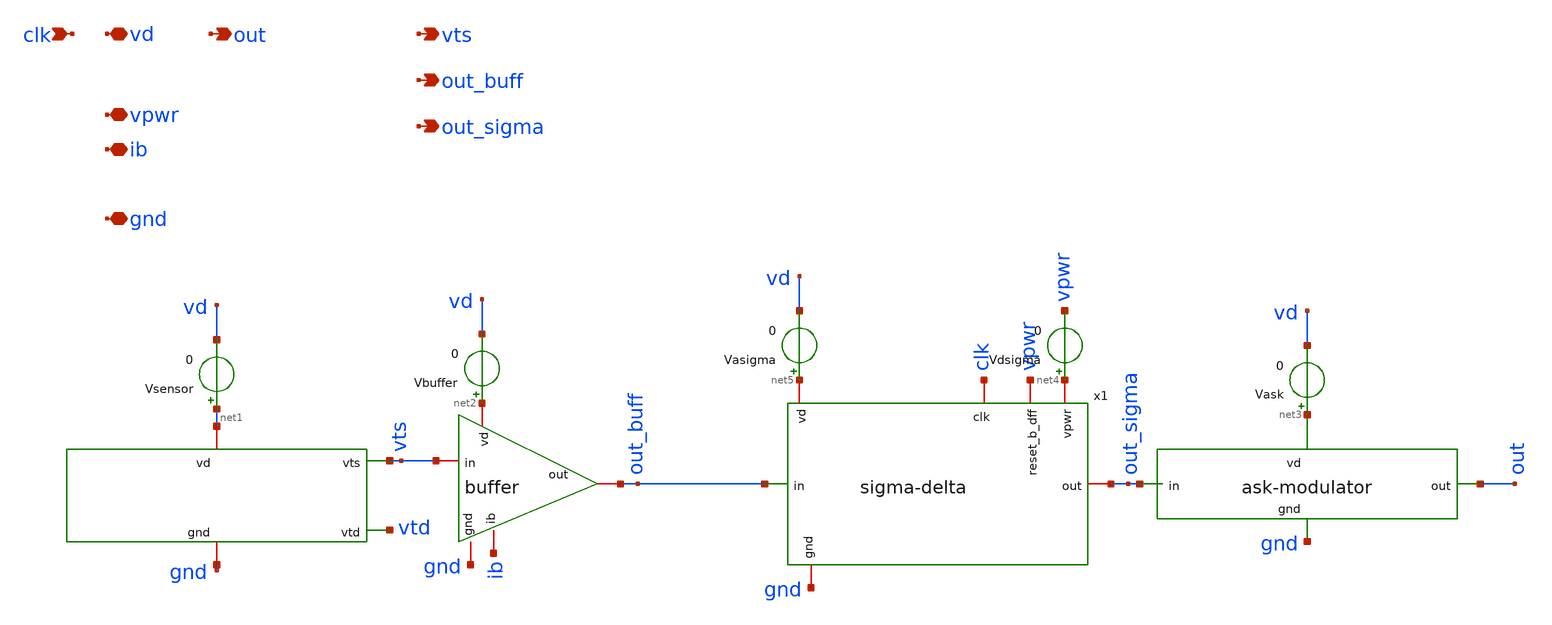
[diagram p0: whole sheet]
** sch_path: device-complete/xschem/device-complete.sch
**.subckt device-complete vd clk out vpwr ib gnd vts out_buff out_sigma
*.iopin vd
*.ipin clk
*.opin out
*.iopin vpwr
*.iopin ib
*.iopin gnd
*.opin vts
*.opin out_buff
*.opin out_sigma
x3 net1 vts vtd gnd sensor
X2 net2 vts out_buff ib gnd buffer
x4 net3 out out_sigma gnd ask-modulator
x1 net4 clk out_sigma out_buff vpwr gnd net5 sigma-delta
Vsensor net1 vd 0
.save i(vsensor)
Vbuffer net2 vd 0
.save i(vbuffer)
Vasigma net5 vd 0
.save i(vasigma)
Vdsigma net4 vpwr 0
.save i(vdsigma)
Vask net3 vd 0
.save i(vask)
**.ends
.end
